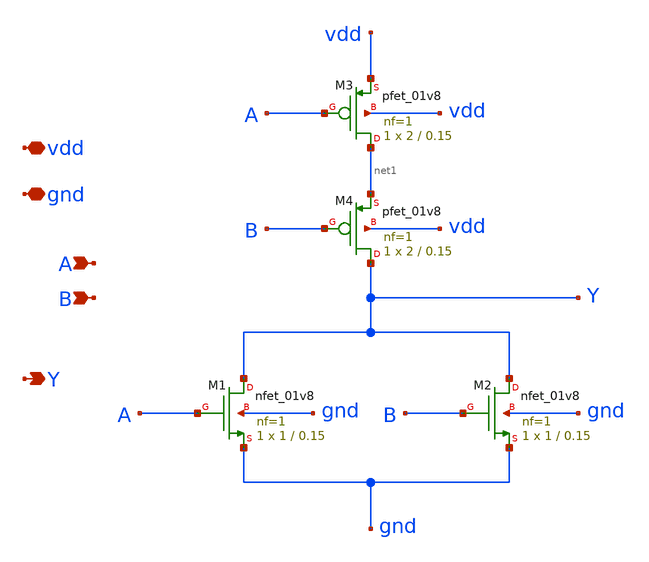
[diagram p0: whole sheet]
** sch_path: LogicGates/nor.sch
**.subckt nor A B vdd gnd Y
*.ipin A
*.ipin B
*.iopin vdd
*.iopin gnd
*.opin Y
XM1 Y A gnd gnd sky130_fd_pr__nfet_01v8 L=0.15 W=1 nf=1 ad='int((nf+1)/2) * W/nf * 0.29' as='int((nf+2)/2) * W/nf * 0.29'
+ pd='2*int((nf+1)/2) * (W/nf + 0.29)' ps='2*int((nf+2)/2) * (W/nf + 0.29)' nrd='0.29 / W' nrs='0.29 / W'
+ sa=0 sb=0 sd=0 mult=1 m=1
XM2 Y B gnd gnd sky130_fd_pr__nfet_01v8 L=0.15 W=1 nf=1 ad='int((nf+1)/2) * W/nf * 0.29' as='int((nf+2)/2) * W/nf * 0.29'
+ pd='2*int((nf+1)/2) * (W/nf + 0.29)' ps='2*int((nf+2)/2) * (W/nf + 0.29)' nrd='0.29 / W' nrs='0.29 / W'
+ sa=0 sb=0 sd=0 mult=1 m=1
XM3 net1 A vdd vdd sky130_fd_pr__pfet_01v8 L=0.15 W=2 nf=1 ad='int((nf+1)/2) * W/nf * 0.29' as='int((nf+2)/2) * W/nf * 0.29'
+ pd='2*int((nf+1)/2) * (W/nf + 0.29)' ps='2*int((nf+2)/2) * (W/nf + 0.29)' nrd='0.29 / W' nrs='0.29 / W'
+ sa=0 sb=0 sd=0 mult=1 m=1
XM4 Y B net1 vdd sky130_fd_pr__pfet_01v8 L=0.15 W=2 nf=1 ad='int((nf+1)/2) * W/nf * 0.29' as='int((nf+2)/2) * W/nf * 0.29'
+ pd='2*int((nf+1)/2) * (W/nf + 0.29)' ps='2*int((nf+2)/2) * (W/nf + 0.29)' nrd='0.29 / W' nrs='0.29 / W'
+ sa=0 sb=0 sd=0 mult=1 m=1
**.ends
.end
